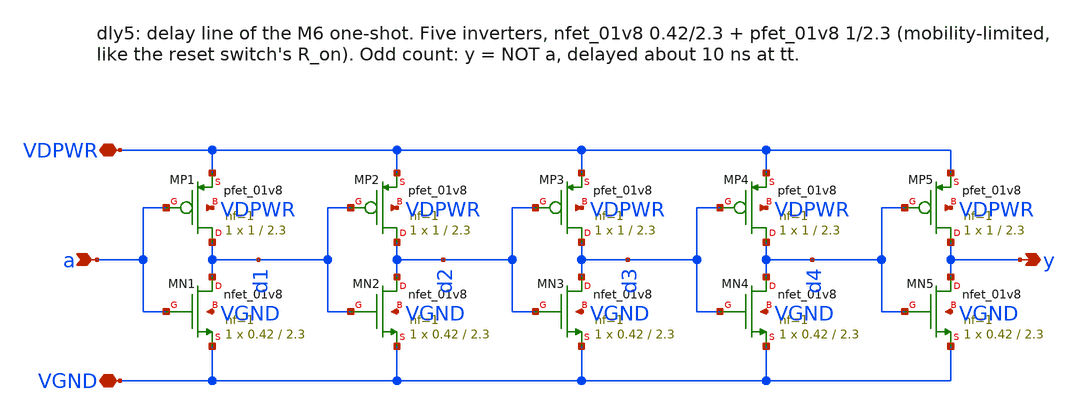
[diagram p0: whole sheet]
** sch_path: xschem/dly5.sch
**.subckt dly5 VDPWR VGND a y
*.iopin VDPWR
*.iopin VGND
*.ipin a
*.opin y
XMP1 d1 a VDPWR VDPWR sky130_fd_pr__pfet_01v8 L=2.3 W=1 nf=1 ad='int((1 + 1)/2) * 1 / 1 * 0.29' as='int((1 + 2)/2) * 1 / 1 * 0.29'
+ pd='2*int((1 + 1)/2) * (1 / 1 + 0.29)' ps='2*int((1 + 2)/2) * (1 / 1 + 0.29)' nrd='0.29 / 1 ' nrs='0.29 / 1 '
+ sa=0 sb=0 sd=0 mult=1 m=1
XMN1 d1 a VGND VGND sky130_fd_pr__nfet_01v8 L=2.3 W=0.42 nf=1 ad='int((1 + 1)/2) * 0.42 / 1 * 0.29' as='int((1 + 2)/2) * 0.42 / 1 * 0.29'
+ pd='2*int((1 + 1)/2) * (0.42 / 1 + 0.29)' ps='2*int((1 + 2)/2) * (0.42 / 1 + 0.29)' nrd='0.29 / 0.42 '
+ nrs='0.29 / 0.42 ' sa=0 sb=0 sd=0 mult=1 m=1
XMP2 d2 d1 VDPWR VDPWR sky130_fd_pr__pfet_01v8 L=2.3 W=1 nf=1 ad='int((1 + 1)/2) * 1 / 1 * 0.29' as='int((1 + 2)/2) * 1 / 1 * 0.29'
+ pd='2*int((1 + 1)/2) * (1 / 1 + 0.29)' ps='2*int((1 + 2)/2) * (1 / 1 + 0.29)' nrd='0.29 / 1 ' nrs='0.29 / 1 '
+ sa=0 sb=0 sd=0 mult=1 m=1
XMN2 d2 d1 VGND VGND sky130_fd_pr__nfet_01v8 L=2.3 W=0.42 nf=1 ad='int((1 + 1)/2) * 0.42 / 1 * 0.29'
+ as='int((1 + 2)/2) * 0.42 / 1 * 0.29' pd='2*int((1 + 1)/2) * (0.42 / 1 + 0.29)' ps='2*int((1 + 2)/2) * (0.42 / 1 + 0.29)'
+ nrd='0.29 / 0.42 ' nrs='0.29 / 0.42 ' sa=0 sb=0 sd=0 mult=1 m=1
XMP3 d3 d2 VDPWR VDPWR sky130_fd_pr__pfet_01v8 L=2.3 W=1 nf=1 ad='int((1 + 1)/2) * 1 / 1 * 0.29' as='int((1 + 2)/2) * 1 / 1 * 0.29'
+ pd='2*int((1 + 1)/2) * (1 / 1 + 0.29)' ps='2*int((1 + 2)/2) * (1 / 1 + 0.29)' nrd='0.29 / 1 ' nrs='0.29 / 1 '
+ sa=0 sb=0 sd=0 mult=1 m=1
XMN3 d3 d2 VGND VGND sky130_fd_pr__nfet_01v8 L=2.3 W=0.42 nf=1 ad='int((1 + 1)/2) * 0.42 / 1 * 0.29'
+ as='int((1 + 2)/2) * 0.42 / 1 * 0.29' pd='2*int((1 + 1)/2) * (0.42 / 1 + 0.29)' ps='2*int((1 + 2)/2) * (0.42 / 1 + 0.29)'
+ nrd='0.29 / 0.42 ' nrs='0.29 / 0.42 ' sa=0 sb=0 sd=0 mult=1 m=1
XMP4 d4 d3 VDPWR VDPWR sky130_fd_pr__pfet_01v8 L=2.3 W=1 nf=1 ad='int((1 + 1)/2) * 1 / 1 * 0.29' as='int((1 + 2)/2) * 1 / 1 * 0.29'
+ pd='2*int((1 + 1)/2) * (1 / 1 + 0.29)' ps='2*int((1 + 2)/2) * (1 / 1 + 0.29)' nrd='0.29 / 1 ' nrs='0.29 / 1 '
+ sa=0 sb=0 sd=0 mult=1 m=1
XMN4 d4 d3 VGND VGND sky130_fd_pr__nfet_01v8 L=2.3 W=0.42 nf=1 ad='int((1 + 1)/2) * 0.42 / 1 * 0.29'
+ as='int((1 + 2)/2) * 0.42 / 1 * 0.29' pd='2*int((1 + 1)/2) * (0.42 / 1 + 0.29)' ps='2*int((1 + 2)/2) * (0.42 / 1 + 0.29)'
+ nrd='0.29 / 0.42 ' nrs='0.29 / 0.42 ' sa=0 sb=0 sd=0 mult=1 m=1
XMP5 y d4 VDPWR VDPWR sky130_fd_pr__pfet_01v8 L=2.3 W=1 nf=1 ad='int((1 + 1)/2) * 1 / 1 * 0.29' as='int((1 + 2)/2) * 1 / 1 * 0.29'
+ pd='2*int((1 + 1)/2) * (1 / 1 + 0.29)' ps='2*int((1 + 2)/2) * (1 / 1 + 0.29)' nrd='0.29 / 1 ' nrs='0.29 / 1 '
+ sa=0 sb=0 sd=0 mult=1 m=1
XMN5 y d4 VGND VGND sky130_fd_pr__nfet_01v8 L=2.3 W=0.42 nf=1 ad='int((1 + 1)/2) * 0.42 / 1 * 0.29' as='int((1 + 2)/2) * 0.42 / 1 * 0.29'
+ pd='2*int((1 + 1)/2) * (0.42 / 1 + 0.29)' ps='2*int((1 + 2)/2) * (0.42 / 1 + 0.29)' nrd='0.29 / 0.42 '
+ nrs='0.29 / 0.42 ' sa=0 sb=0 sd=0 mult=1 m=1
**.ends
.end
